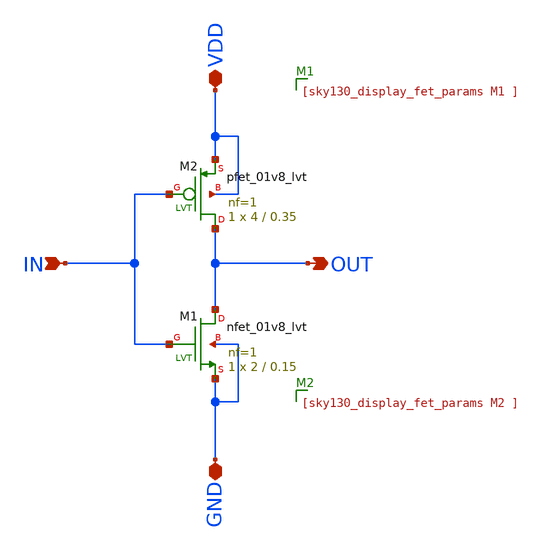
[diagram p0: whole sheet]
** sch_path: 05_mixed_signal/soluzioni/lab03/xschem/inverter.sch
**.subckt inverter IN OUT VDD GND
*.ipin IN
*.opin OUT
*.iopin VDD
*.iopin GND
XM1 OUT IN GND GND sky130_fd_pr__nfet_01v8_lvt L=0.15 W=2 nf=1 ad='int((1 + 1)/2) * 2 / 1 * 0.29' as='int((1 + 2)/2) * 2 / 1 * 0.29'
+ pd='2*int((1 + 1)/2) * (2 / 1 + 0.29)' ps='2*int((1 + 2)/2) * (2 / 1 + 0.29)' nrd='0.29 / 2 ' nrs='0.29 / 2 '
+ sa=0 sb=0 sd=0 mult=1 m=1
XM2 OUT IN VDD VDD sky130_fd_pr__pfet_01v8_lvt L=0.35 W=4 nf=1 ad='int((1 + 1)/2) * 4 / 1 * 0.29' as='int((1 + 2)/2) * 4 / 1 * 0.29'
+ pd='2*int((1 + 1)/2) * (4 / 1 + 0.29)' ps='2*int((1 + 2)/2) * (4 / 1 + 0.29)' nrd='0.29 / 4 ' nrs='0.29 / 4 '
+ sa=0 sb=0 sd=0 mult=1 m=1
**.ends
.end
